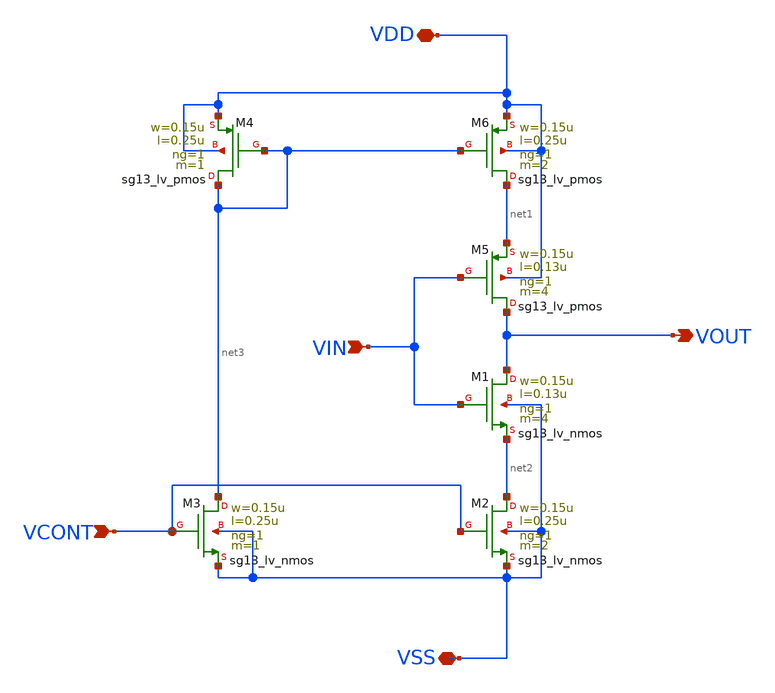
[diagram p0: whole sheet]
** sch_path: PhaseInterpolator/2to4/delay_variable.sch
**.subckt delay_variable VSS VDD VOUT VCONT VIN
*.iopin VSS
*.iopin VDD
*.opin VOUT
*.ipin VCONT
*.ipin VIN
XM1 VOUT VIN net2 VSS sg13_lv_nmos w=0.15u l=0.13u ng=1 m=4 mm_ok=1
XM2 net2 VCONT VSS VSS sg13_lv_nmos w=0.15u l=0.25u ng=1 m=2 mm_ok=1
XM3 net3 VCONT VSS VSS sg13_lv_nmos w=0.15u l=0.25u ng=1 m=1 mm_ok=1
XM5 VOUT VIN net1 VDD sg13_lv_pmos w=0.15u l=0.13u ng=1 m=4 mm_ok=1
XM6 net1 net3 VDD VDD sg13_lv_pmos w=0.15u l=0.25u ng=1 m=2 mm_ok=1
XM4 net3 net3 VDD VDD sg13_lv_pmos w=0.15u l=0.25u ng=1 m=1 mm_ok=1
**.ends
.end
